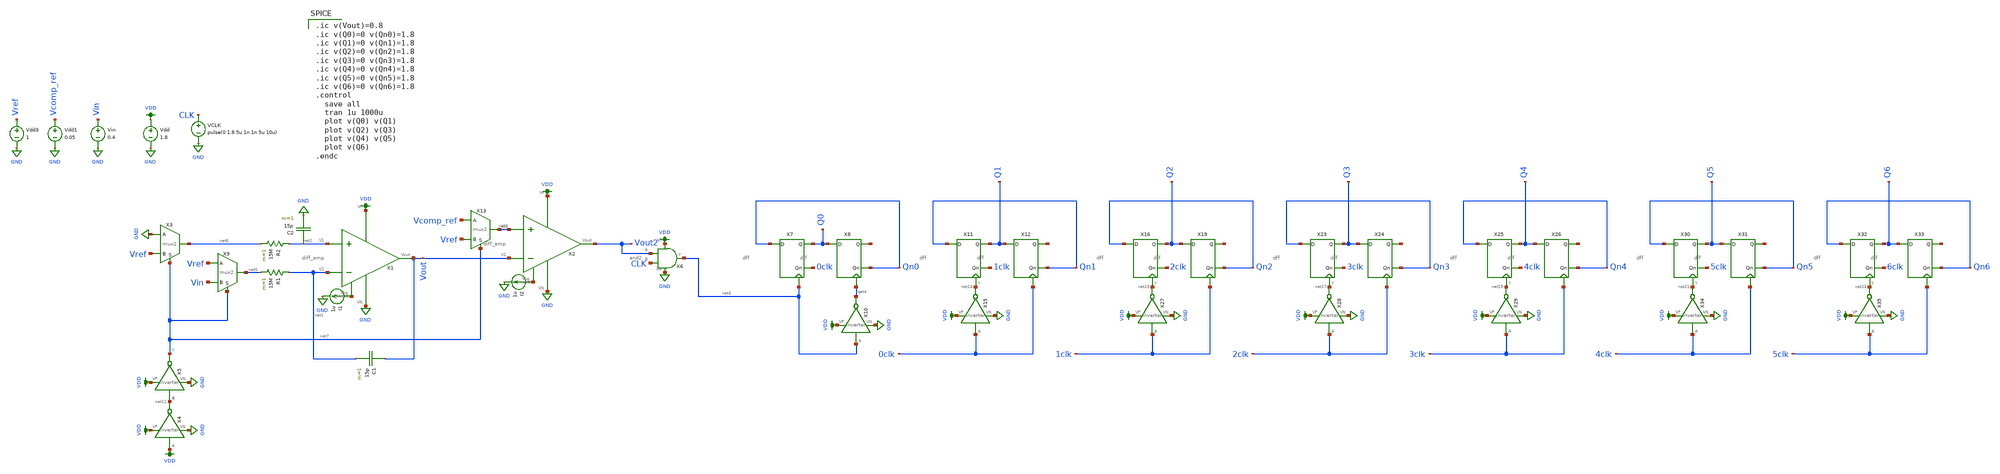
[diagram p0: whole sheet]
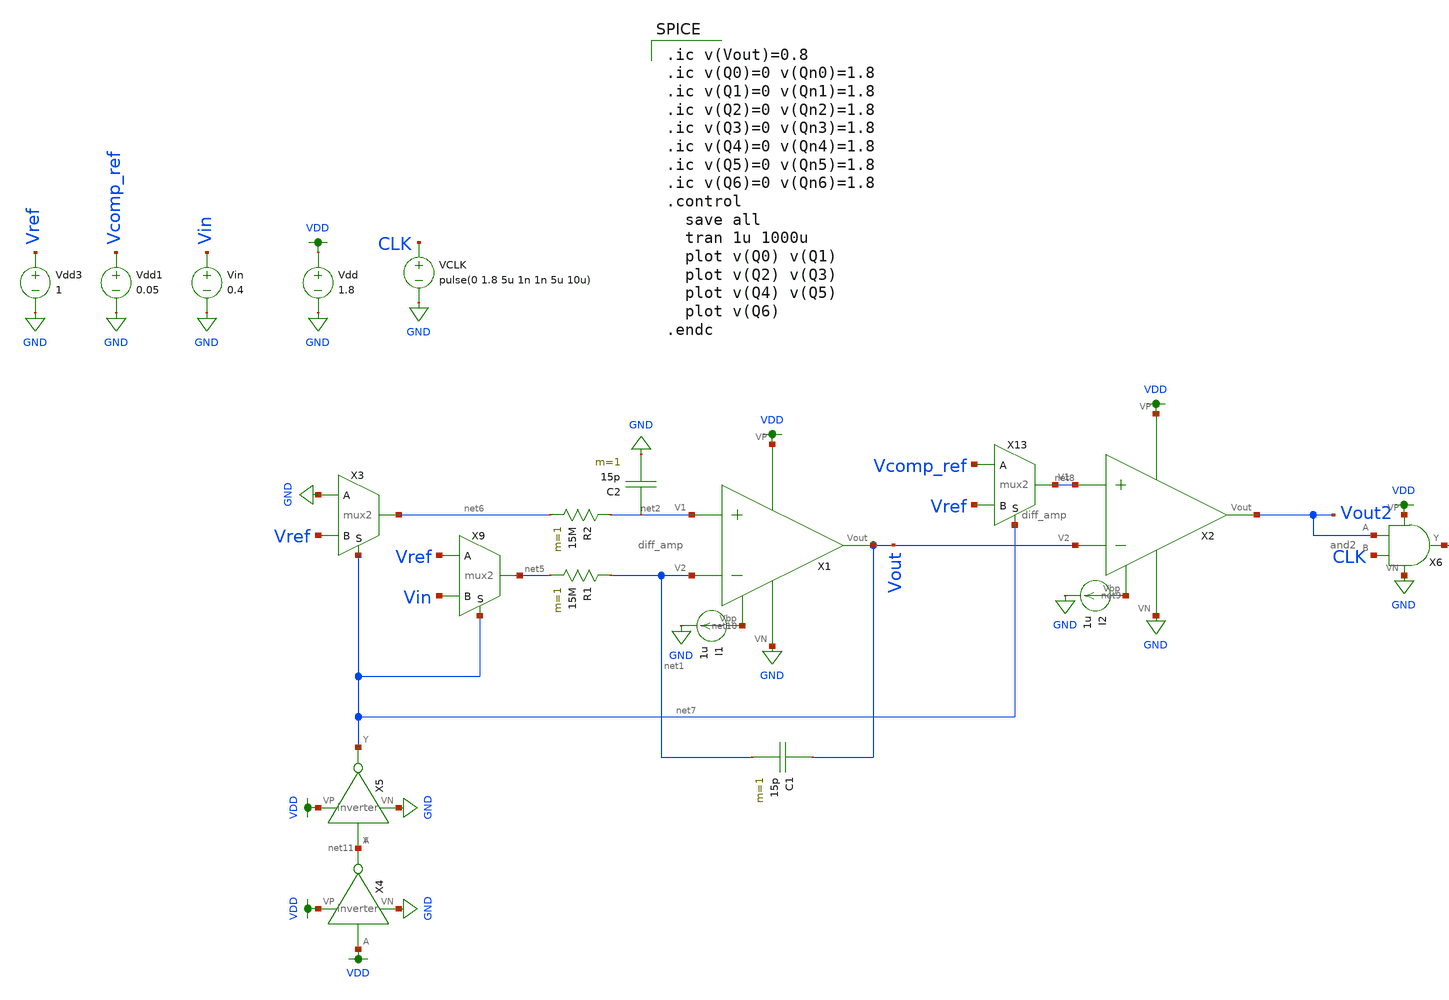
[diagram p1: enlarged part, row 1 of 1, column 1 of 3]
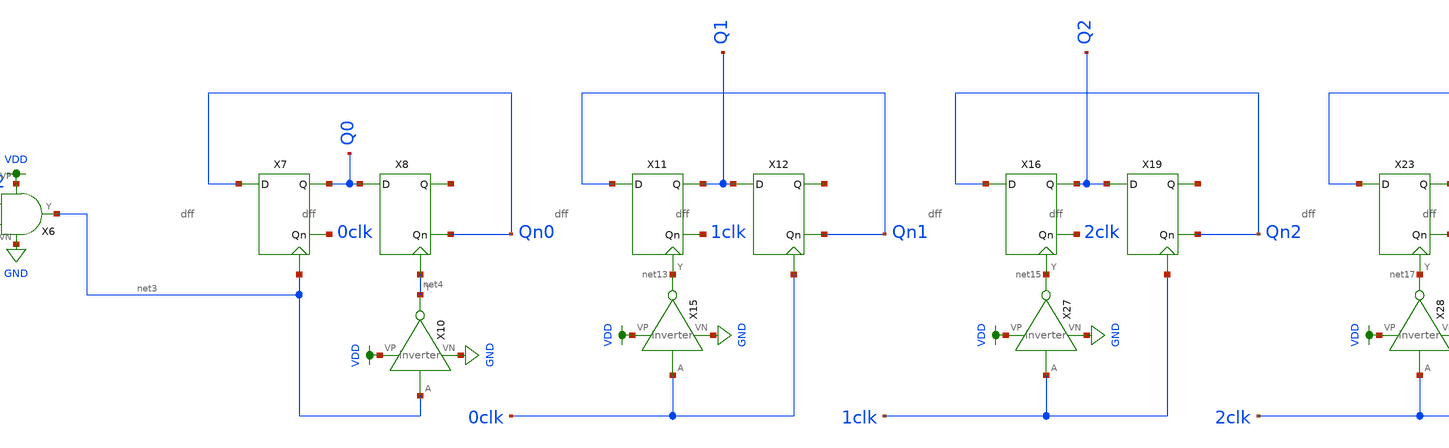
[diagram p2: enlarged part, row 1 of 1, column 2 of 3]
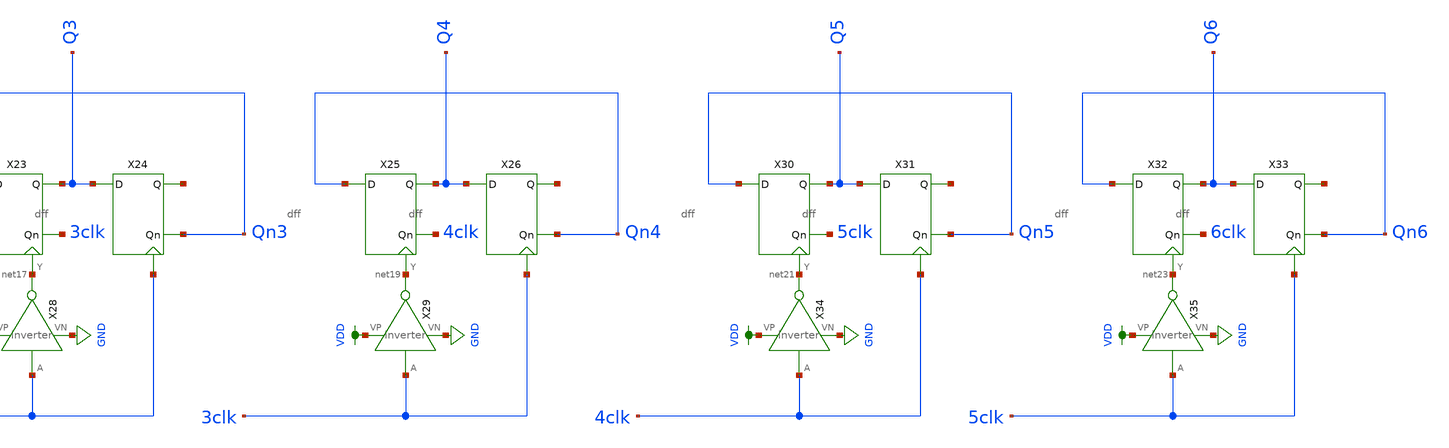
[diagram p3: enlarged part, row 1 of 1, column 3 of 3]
** sch_path: schematic/double-slope-thomas_new.sch
**.subckt double-slope-thomas_new
X2 VDD net9 Vout2 net8 Vout GND diff_amp
Vdd VDD GND 1.8
VCLK CLK GND pulse(0 1.8 5u 1n 1n 5u 10u)
Vdd1 Vcomp_ref GND 0.05
Vin Vin GND 0.4
I2 net9 GND 1u
C1 Vout net1 15p m=1
X1 VDD net10 Vout net2 net1 GND diff_amp
R1 net1 net5 15M m=1
C2 net2 GND 15p m=1
R2 net2 net6 15M m=1
I1 net10 GND 1u
Vdd3 Vref GND 1
X4 VDD net11 VDD GND inverter
X5 net11 net7 VDD GND inverter
X6 VDD Vout2 GND net3 CLK and2
X7 Qn0 0clk Q0 net3 dff
X8 Q0 Qn0 net12 net4 dff
X10 net3 net4 VDD GND inverter
X11 Qn1 1clk Q1 net13 dff
X12 Q1 Qn1 net14 0clk dff
X15 0clk net13 VDD GND inverter
X16 Qn2 2clk Q2 net15 dff
X19 Q2 Qn2 net16 1clk dff
X23 Qn3 3clk Q3 net17 dff
X24 Q3 Qn3 net18 2clk dff
X25 Qn4 4clk Q4 net19 dff
X26 Q4 Qn4 net20 3clk dff
X27 1clk net15 VDD GND inverter
X28 2clk net17 VDD GND inverter
X29 3clk net19 VDD GND inverter
X30 Qn5 5clk Q5 net21 dff
X31 Q5 Qn5 net22 4clk dff
X32 Qn6 6clk Q6 net23 dff
X33 Q6 Qn6 net24 5clk dff
X34 4clk net21 VDD GND inverter
X35 5clk net23 VDD GND inverter
X3 net6 GND Vref net7 mux2
X9 net5 Vref Vin net7 mux2
X13 net8 Vcomp_ref Vref net7 mux2
**** begin user architecture code

.ic v(Vout)=0.8
.ic v(Q0)=0 v(Qn0)=1.8
.ic v(Q1)=0 v(Qn1)=1.8
.ic v(Q2)=0 v(Qn2)=1.8
.ic v(Q3)=0 v(Qn3)=1.8
.ic v(Q4)=0 v(Qn4)=1.8
.ic v(Q5)=0 v(Qn5)=1.8
.ic v(Q6)=0 v(Qn6)=1.8
.control
  save all
  tran 1u 1000u
  plot v(Q0) v(Q1)
  plot v(Q2) v(Q3)
  plot v(Q4) v(Q5)
  plot v(Q6)
.endc


.option wnflag=1
.param MC_SWITCH=0.0
.lib ~/skywater/skywater-pdk/libraries/sky130_fd_pr_ngspice/latest/models/sky130.lib.spice tt

**** end user architecture code
**.ends
.GLOBAL GND
.GLOBAL VDD
.end
